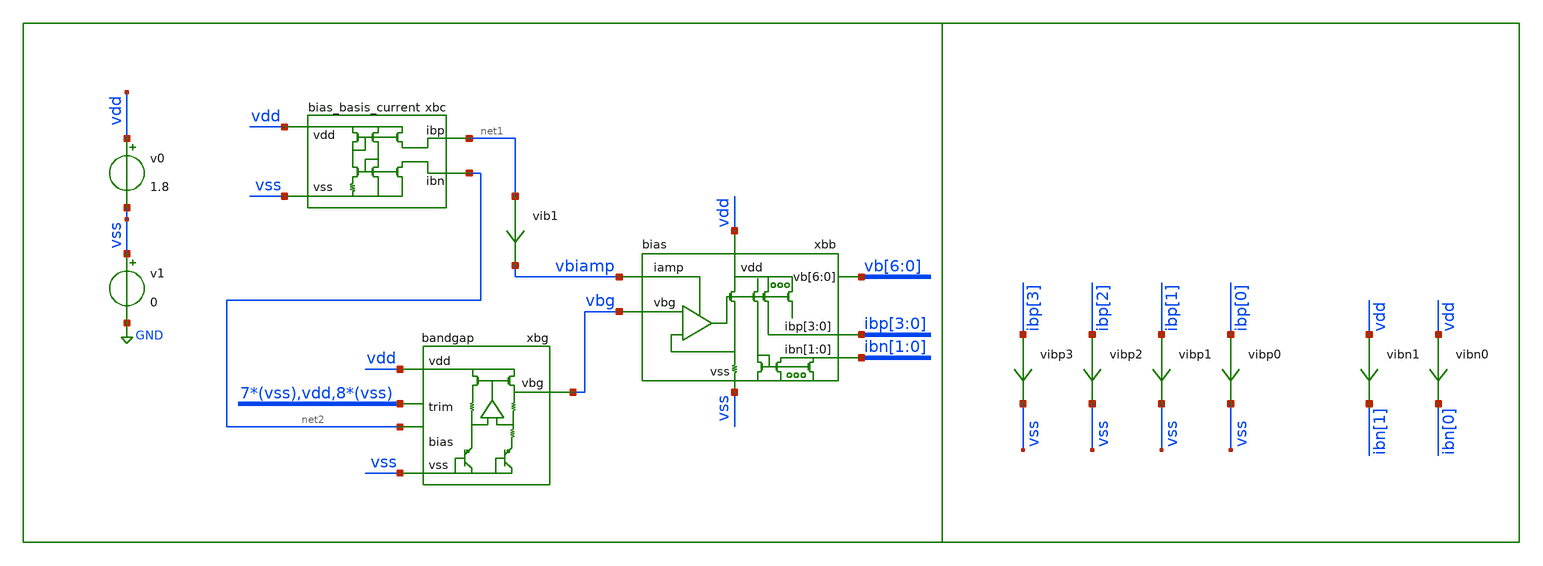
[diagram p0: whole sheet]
** sch_path: xschem/tb/bias/dc_bias.sch
**.subckt dc_bias
v0 vdd vss 1.8
v1 vss GND 0
xbb vbiamp vbg ibp[3] ibp[2] ibp[1] ibp[0] ibn[1] ibn[0] vdd vss vb[6] vb[5] vb[4] vb[3] vb[2] vb[1]
+ vb[0] bias
vib1 net1 vbiamp 0
.save i(vib1)
xbc vdd vss net1 net2 bias_basis_current
vibp3 ibp[3] vss 0
.save i(vibp3)
vibp1 ibp[1] vss 0
.save i(vibp1)
vibp2 ibp[2] vss 0
.save i(vibp2)
vibp0 ibp[0] vss 0
.save i(vibp0)
xbg vdd vbg vss net2 vss vss vss vss vss vss vss vdd vss vss vss vss vss vss vss vss bandgap
vibn1 vdd ibn[1] 0
.save i(vibn1)
vibn0 vdd ibn[0] 0
.save i(vibn0)
**** begin user architecture code

.control
.param MC_SWITCH=0

save all
op

*echo -----------------
*show m.xbb.xm1.msky130_fd_pr__pfet_01v8_lvt

echo -----------------
print vb_0_
print vb_1_
print vb_2_
print vb_3_
print vb_4_
print vb_5_
print vb_6_

print vibp0#branch
print vibp1#branch
print vibp2#branch
print vibp3#branch

print vibn0#branch
print vibn1#branch

print v.xbb.vbase#branch
print v.xbb.vm1#branch
print v.xbb.vm1#branch
echo -----------------

*dc temp -10 75 0.1
*plot vibp0#branch
*plot vibp1#branch
*plot vbg
* tran 1n 10u
.endc


 .include $::SKYWATER_STDCELLS/cells/inv/sky130_fd_sc_hd__inv_1.spice

* FET CORNERS
.include $::SKYWATER_MODELS/corners/tt.spice
*.include $::SKYWATER_MODELS/corners/ff.spice
*.include $::SKYWATER_MODELS/corners/ss.spice
*.include $::SKYWATER_MODELS/corners/sf.spice
*.include $::SKYWATER_MODELS/corners/fs.spice

* TT + R + C
*.include $::SKYWATER_MODELS/corners/tt_rmax_cmax.spice
*.include $::SKYWATER_MODELS/corners/tt_rmin_cmin.spice
*.include $::SKYWATER_MODELS/corners/tt_rmax_cmin.spice
*.include $::SKYWATER_MODELS/corners/tt_rmin_cmax.spice

* FF + R + C
*.include $::SKYWATER_MODELS/corners/ff_rmax_cmax.spice
*.include $::SKYWATER_MODELS/corners/ff_rmin_cmin.spice
*.include $::SKYWATER_MODELS/corners/ff_rmax_cmin.spice
*.include $::SKYWATER_MODELS/corners/ff_rmin_cmax.spice


* SS + R + C
*.include $::SKYWATER_MODELS/corners/ss_rmax_cmax.spice
*.include $::SKYWATER_MODELS/corners/ss_rmin_cmin.spice
*.include $::SKYWATER_MODELS/corners/ss_rmax_cmin.spice
*.include $::SKYWATER_MODELS/corners/ss_rmin_cmax.spice

* SF + R + C
*.include $::SKYWATER_MODELS/corners/sf_rmax_cmax.spice
*.include $::SKYWATER_MODELS/corners/sf_rmin_cmin.spice
*.include $::SKYWATER_MODELS/corners/sf_rmax_cmin.spice
*.include $::SKYWATER_MODELS/corners/sf_rmin_cmax.spice

* FS + R + C
*.include $::SKYWATER_MODELS/corners/fs_rmax_cmax.spice
*.include $::SKYWATER_MODELS/corners/fs_rmin_cmin.spice
*.include $::SKYWATER_MODELS/corners/fs_rmax_cmin.spice
*.include $::SKYWATER_MODELS/corners/fs_rmin_cmax.spice

**** end user architecture code
**.ends
.GLOBAL GND
.end
